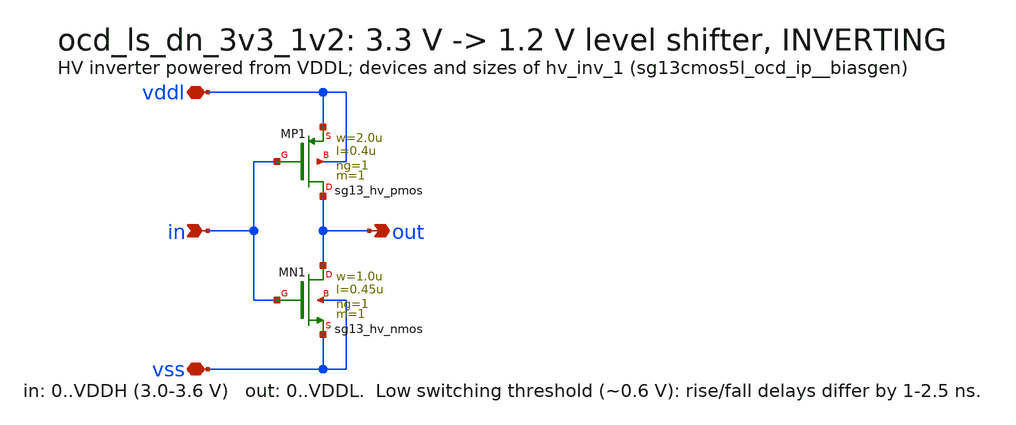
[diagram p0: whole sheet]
** sch_path: macros/ocd_ls_dn_3v3_1v2/schematic/xschem/ocd_ls_dn_3v3_1v2.sch
**.subckt ocd_ls_dn_3v3_1v2 vss vddl out in
*.iopin vss
*.iopin vddl
*.opin out
*.ipin in
XMP1 out in vddl vddl sg13_hv_pmos w=2.0u l=0.4u ng=1 m=1 mm_ok=1
XMN1 out in vss vss sg13_hv_nmos w=1.0u l=0.45u ng=1 m=1 mm_ok=1
**.ends
.end
